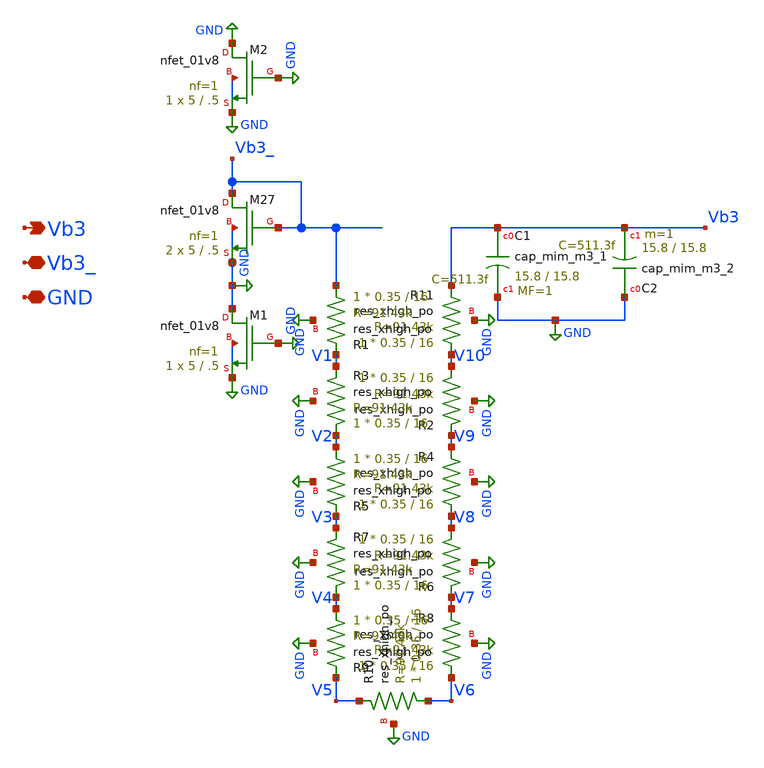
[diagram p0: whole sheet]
** sch_path: xschem/mirror_3.sch
**.subckt mirror_3 GND Vb3_ Vb3
*.iopin GND
*.iopin Vb3_
*.opin Vb3
XM27 Vb3_ Vb3_ GND GND sky130_fd_pr__nfet_01v8 L=.5 W=5 nf=1 ad='int((nf+1)/2) * W/nf * 0.29' as='int((nf+2)/2) * W/nf * 0.29'
+ pd='2*int((nf+1)/2) * (W/nf + 0.29)' ps='2*int((nf+2)/2) * (W/nf + 0.29)' nrd='0.29 / W' nrs='0.29 / W'
+ sa=0 sb=0 sd=0 mult=2 m=2
XR11 V10 Vb3 GND sky130_fd_pr__res_xhigh_po W=0.35 L=16 mult=1 m=1
XC1 Vb3 GND sky130_fd_pr__cap_mim_m3_1 W=15.8 L=15.8 MF=1 m=1
XC2 GND Vb3 sky130_fd_pr__cap_mim_m3_2 W=15.8 L=15.8 MF=1 m=1
XR1 Vb3_ V1 GND sky130_fd_pr__res_xhigh_po W=0.35 L=16 mult=1 m=1
XR2 V10 V9 GND sky130_fd_pr__res_xhigh_po W=0.35 L=16 mult=1 m=1
XR3 V2 V1 GND sky130_fd_pr__res_xhigh_po W=0.35 L=16 mult=1 m=1
XR4 V8 V9 GND sky130_fd_pr__res_xhigh_po W=0.35 L=16 mult=1 m=1
XR5 V2 V3 GND sky130_fd_pr__res_xhigh_po W=0.35 L=16 mult=1 m=1
XR6 V8 V7 GND sky130_fd_pr__res_xhigh_po W=0.35 L=16 mult=1 m=1
XR7 V4 V3 GND sky130_fd_pr__res_xhigh_po W=0.35 L=16 mult=1 m=1
XR8 V6 V7 GND sky130_fd_pr__res_xhigh_po W=0.35 L=16 mult=1 m=1
XR9 V4 V5 GND sky130_fd_pr__res_xhigh_po W=0.35 L=16 mult=1 m=1
XR10 V6 V5 GND sky130_fd_pr__res_xhigh_po W=0.35 L=16 mult=1 m=1
XM1 GND GND GND GND sky130_fd_pr__nfet_01v8 L=.5 W=5 nf=1 ad='int((nf+1)/2) * W/nf * 0.29' as='int((nf+2)/2) * W/nf * 0.29'
+ pd='2*int((nf+1)/2) * (W/nf + 0.29)' ps='2*int((nf+2)/2) * (W/nf + 0.29)' nrd='0.29 / W' nrs='0.29 / W'
+ sa=0 sb=0 sd=0 mult=1 m=1
XM2 GND GND GND GND sky130_fd_pr__nfet_01v8 L=.5 W=5 nf=1 ad='int((nf+1)/2) * W/nf * 0.29' as='int((nf+2)/2) * W/nf * 0.29'
+ pd='2*int((nf+1)/2) * (W/nf + 0.29)' ps='2*int((nf+2)/2) * (W/nf + 0.29)' nrd='0.29 / W' nrs='0.29 / W'
+ sa=0 sb=0 sd=0 mult=1 m=1
**.ends
.GLOBAL GND
.end
